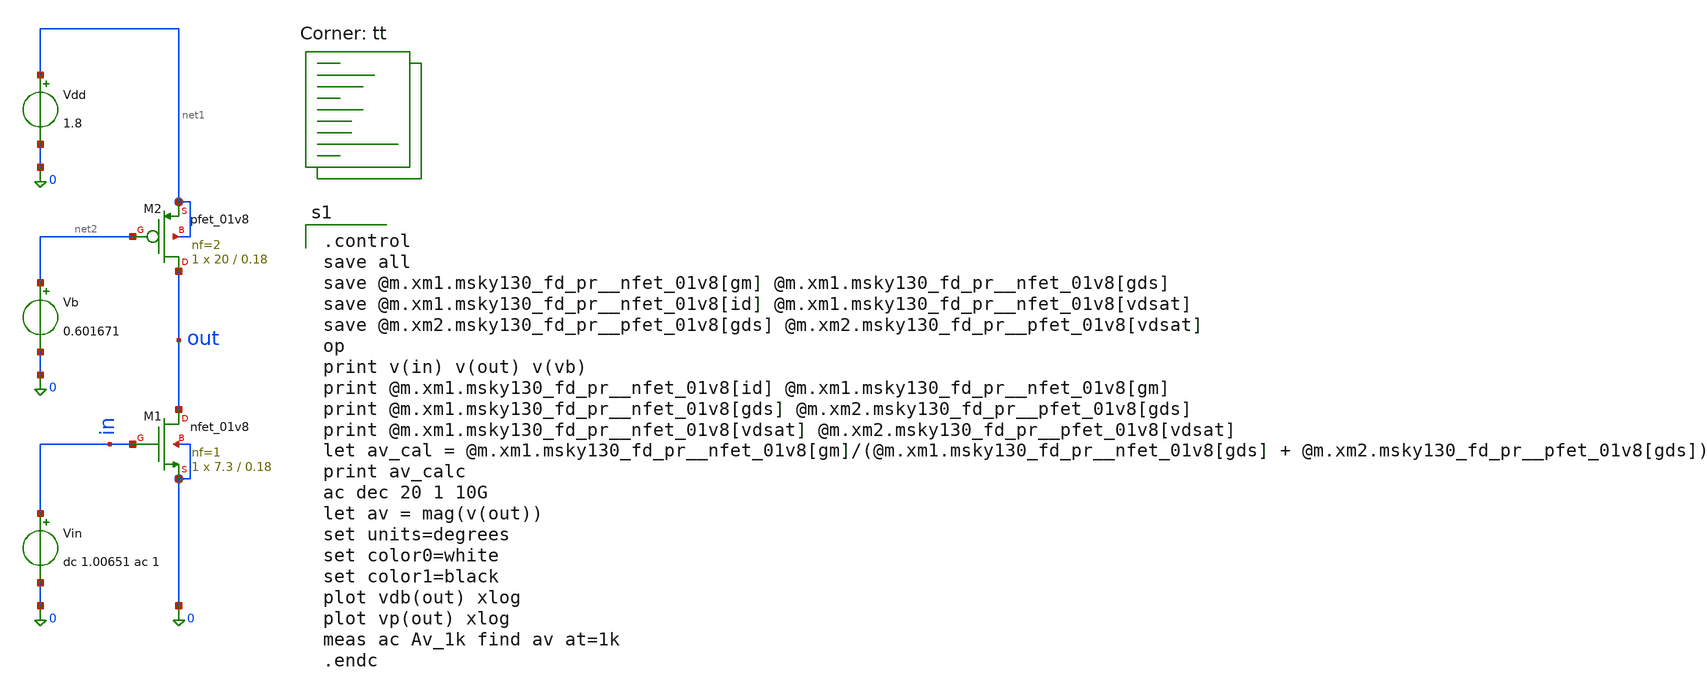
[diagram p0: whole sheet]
** sch_path: Homework 6 - Simulation on Open Source Softwares/Simulations/ex5_final.sch
**.subckt ex5_final
Vin in 0 dc 1.00651 ac 1
XM1 out in 0 0 sky130_fd_pr__nfet_01v8 L=0.18 W=7.3 nf=1 ad='int((1 + 1)/2) * 7.3 / 1 * 0.29' as='int((1 + 2)/2) * 7.3 / 1 * 0.29'
+ pd='2*int((1 + 1)/2) * (7.3 / 1 + 0.29)' ps='2*int((1 + 2)/2) * (7.3 / 1 + 0.29)' nrd='0.29 / 7.3 ' nrs='0.29 / 7.3 '
+ sa=0 sb=0 sd=0 mult=1 m=1
XM2 out net2 net1 net1 sky130_fd_pr__pfet_01v8 L=0.18 W=20 nf=2 ad='int((2 + 1)/2) * 20 / 2 * 0.29' as='int((2 + 2)/2) * 20 / 2 * 0.29'
+ pd='2*int((2 + 1)/2) * (20 / 2 + 0.29)' ps='2*int((2 + 2)/2) * (20 / 2 + 0.29)' nrd='0.29 / 20 ' nrs='0.29 / 20 '
+ sa=0 sb=0 sd=0 mult=1 m=1
Vdd net1 0 1.8
Vb net2 0 0.601671
**** begin user architecture code
.lib $::SKYWATER_MODELS/sky130.lib.spice tt

.control
save all
save @m.xm1.msky130_fd_pr__nfet_01v8[gm] @m.xm1.msky130_fd_pr__nfet_01v8[gds]
save @m.xm1.msky130_fd_pr__nfet_01v8[id] @m.xm1.msky130_fd_pr__nfet_01v8[vdsat]
save @m.xm2.msky130_fd_pr__pfet_01v8[gds] @m.xm2.msky130_fd_pr__pfet_01v8[vdsat]
op
print v(in) v(out) v(vb)
print @m.xm1.msky130_fd_pr__nfet_01v8[id] @m.xm1.msky130_fd_pr__nfet_01v8[gm]
print @m.xm1.msky130_fd_pr__nfet_01v8[gds] @m.xm2.msky130_fd_pr__pfet_01v8[gds]
print @m.xm1.msky130_fd_pr__nfet_01v8[vdsat] @m.xm2.msky130_fd_pr__pfet_01v8[vdsat]
let av_cal = @m.xm1.msky130_fd_pr__nfet_01v8[gm]/(@m.xm1.msky130_fd_pr__nfet_01v8[gds] +
+ @m.xm2.msky130_fd_pr__pfet_01v8[gds])
print av_calc
ac dec 20 1 10G
let av = mag(v(out))
set units=degrees
set color0=white
set color1=black
plot vdb(out) xlog
plot vp(out) xlog
meas ac Av_1k find av at=1k
.endc


**** end user architecture code
**.ends
.end
